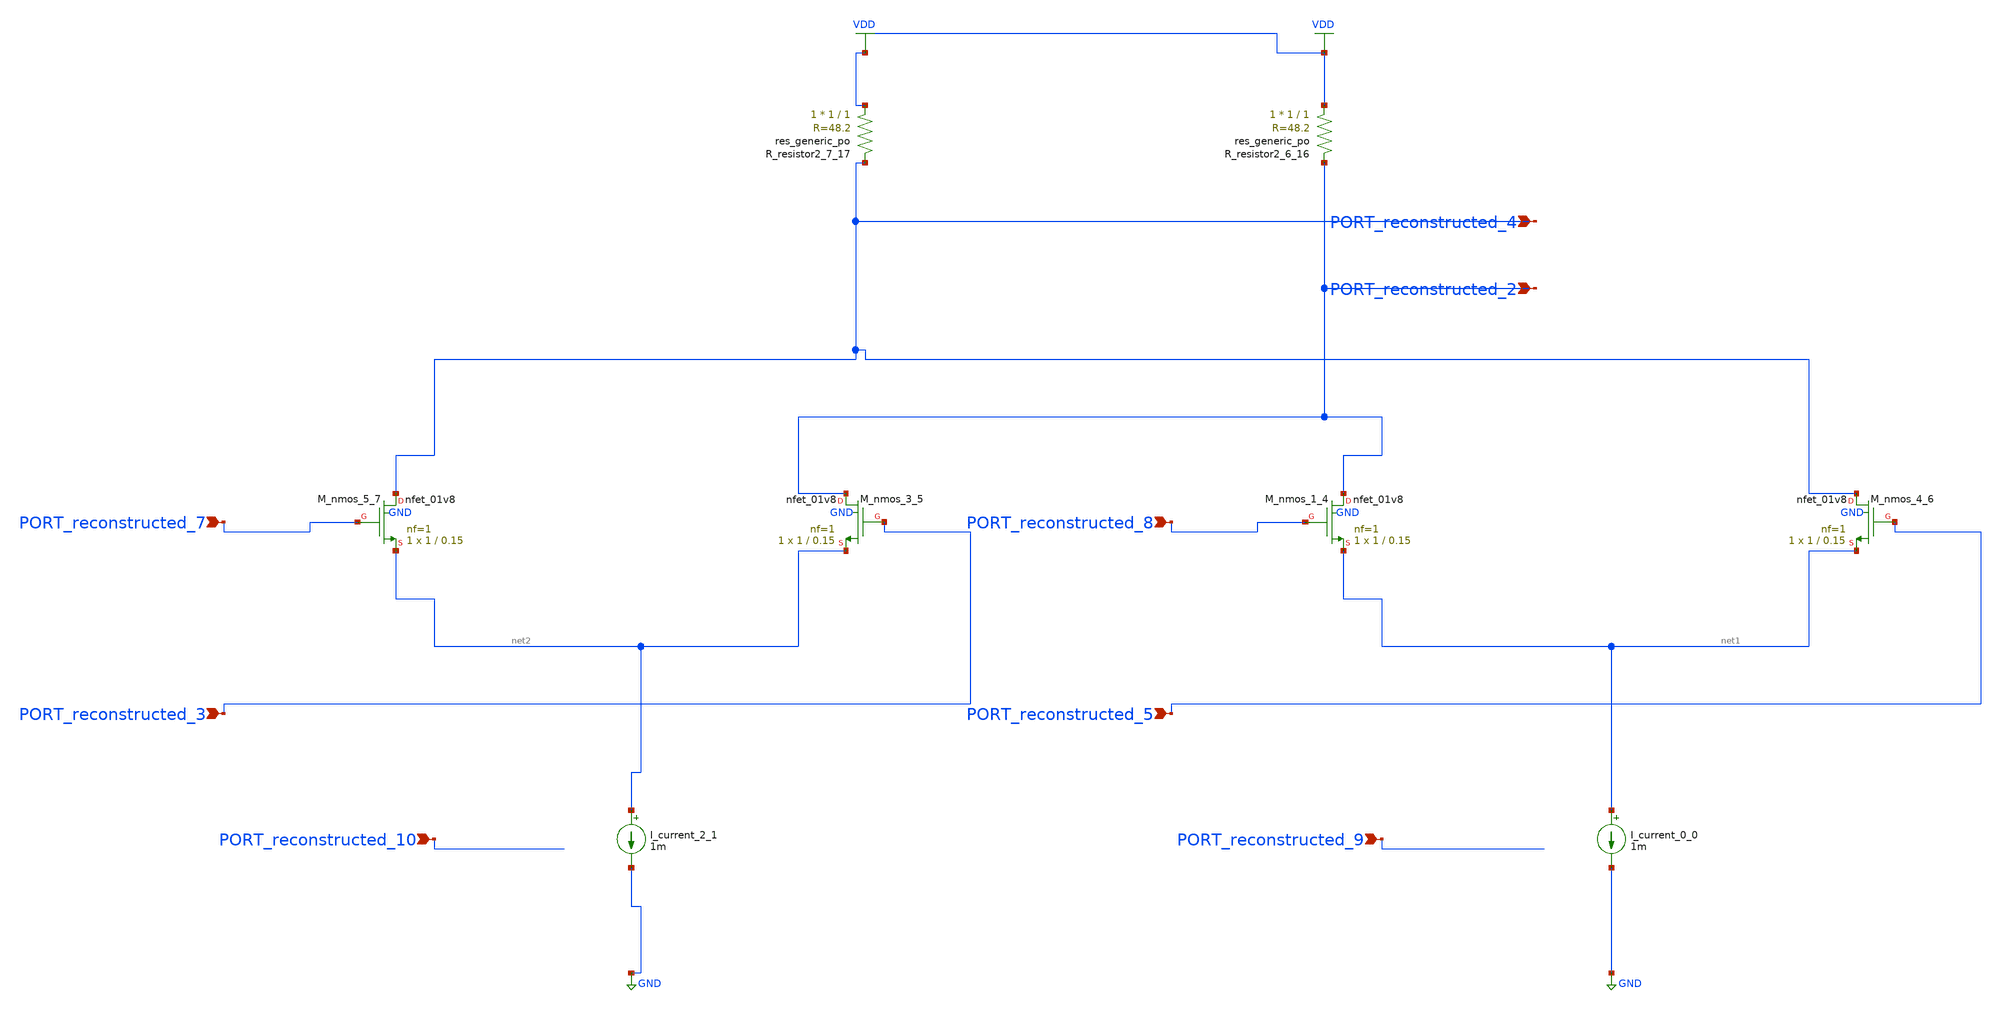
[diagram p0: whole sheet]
** sch_path: schematics/AMSNet/231.sch
**.subckt 231 PORT_reconstructed_8 PORT_reconstructed_5 PORT_reconstructed_3 PORT_reconstructed_7
*+ PORT_reconstructed_2 PORT_reconstructed_4 PORT_reconstructed_9 PORT_reconstructed_10
*.ipin PORT_reconstructed_8
*.ipin PORT_reconstructed_5
*.ipin PORT_reconstructed_3
*.ipin PORT_reconstructed_7
*.ipin PORT_reconstructed_2
*.ipin PORT_reconstructed_4
*.ipin PORT_reconstructed_9
*.ipin PORT_reconstructed_10
I_current_0_0 net1 GND 1m
I_current_2_1 net2 GND 1m
XM_nmos_1_4 PORT_reconstructed_2 PORT_reconstructed_8 net1 GND sky130_fd_pr__nfet_01v8 L=0.15 W=1 nf=1
+ ad='int((1 + 1)/2) * 1 / 1 * 0.29' as='int((1 + 2)/2) * 1 / 1 * 0.29' pd='2*int((1 + 1)/2) * (1 / 1 + 0.29)'
+ ps='2*int((1 + 2)/2) * (1 / 1 + 0.29)' nrd='0.29 / 1 ' nrs='0.29 / 1 ' sa=0 sb=0 sd=0 mult=1 m=1
XM_nmos_3_5 PORT_reconstructed_2 PORT_reconstructed_3 net2 GND sky130_fd_pr__nfet_01v8 L=0.15 W=1 nf=1
+ ad='int((1 + 1)/2) * 1 / 1 * 0.29' as='int((1 + 2)/2) * 1 / 1 * 0.29' pd='2*int((1 + 1)/2) * (1 / 1 + 0.29)'
+ ps='2*int((1 + 2)/2) * (1 / 1 + 0.29)' nrd='0.29 / 1 ' nrs='0.29 / 1 ' sa=0 sb=0 sd=0 mult=1 m=1
XM_nmos_4_6 PORT_reconstructed_4 PORT_reconstructed_5 net1 GND sky130_fd_pr__nfet_01v8 L=0.15 W=1 nf=1
+ ad='int((1 + 1)/2) * 1 / 1 * 0.29' as='int((1 + 2)/2) * 1 / 1 * 0.29' pd='2*int((1 + 1)/2) * (1 / 1 + 0.29)'
+ ps='2*int((1 + 2)/2) * (1 / 1 + 0.29)' nrd='0.29 / 1 ' nrs='0.29 / 1 ' sa=0 sb=0 sd=0 mult=1 m=1
XM_nmos_5_7 PORT_reconstructed_4 PORT_reconstructed_7 net2 GND sky130_fd_pr__nfet_01v8 L=0.15 W=1 nf=1
+ ad='int((1 + 1)/2) * 1 / 1 * 0.29' as='int((1 + 2)/2) * 1 / 1 * 0.29' pd='2*int((1 + 1)/2) * (1 / 1 + 0.29)'
+ ps='2*int((1 + 2)/2) * (1 / 1 + 0.29)' nrd='0.29 / 1 ' nrs='0.29 / 1 ' sa=0 sb=0 sd=0 mult=1 m=1
XR_resistor2_6_16 VDD PORT_reconstructed_2 sky130_fd_pr__res_generic_po W=1 L=1 m=1
XR_resistor2_7_17 VDD PORT_reconstructed_4 sky130_fd_pr__res_generic_po W=1 L=1 m=1
**.ends
.GLOBAL GND
.GLOBAL VDD
.end
